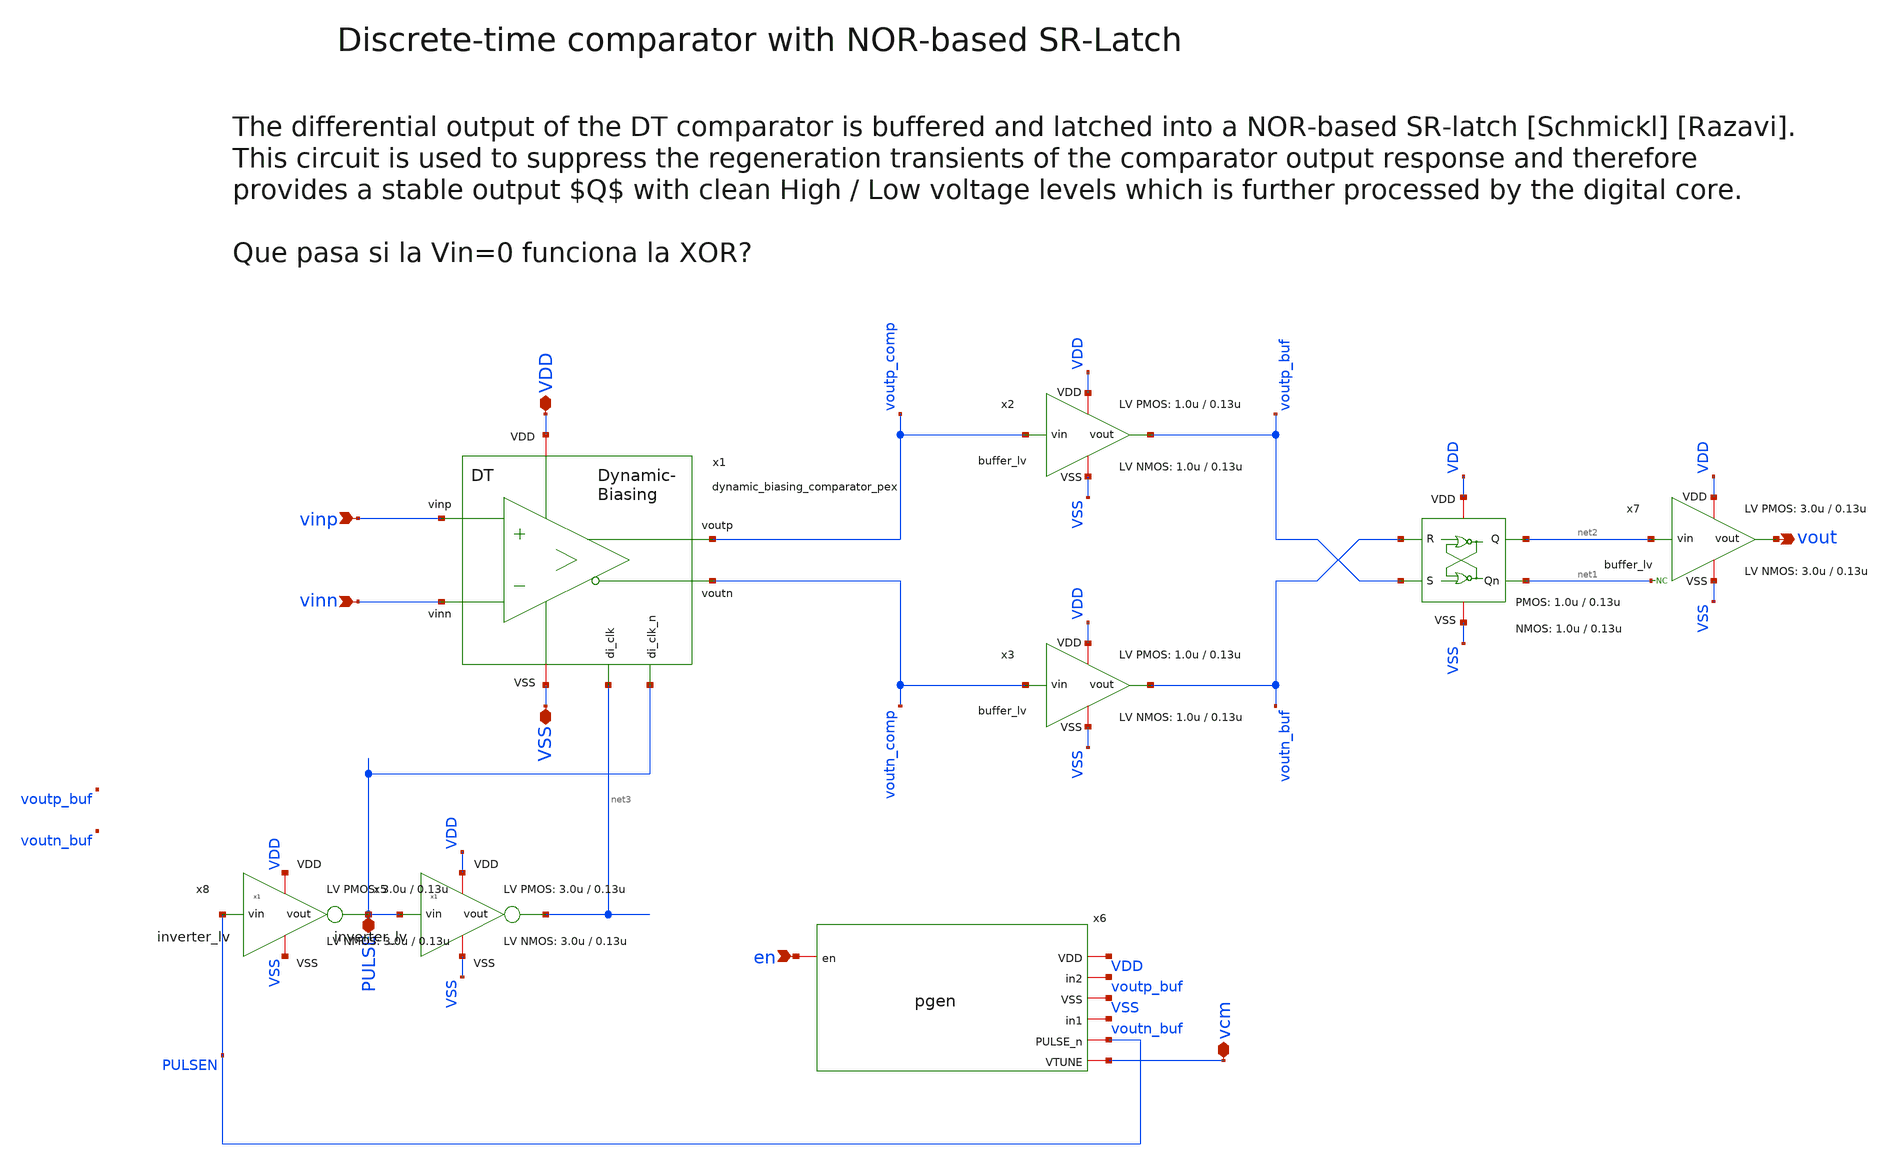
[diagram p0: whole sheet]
** sch_path: xschem/comparator/discrete_time/DT_comparator.sch
**.subckt DT_comparator VDD vout VSS vinp vinn en PULSE vcm
*.iopin VDD
*.opin vout
*.iopin VSS
*.ipin vinp
*.ipin vinn
*.ipin en
*.iopin PULSE
*.iopin vcm
x2 VDD voutp_comp voutp_buf VSS buffer_lv W_P_INV=1.0u L_P_INV=0.13u W_N_INV=1.0u L_N_INV=0.13u
x3 VDD voutn_comp voutn_buf VSS buffer_lv W_P_INV=1.0u L_P_INV=0.13u W_N_INV=1.0u L_N_INV=0.13u
x5 VDD PULSE net3 VSS inverter_lv W_P=3.0u L_P=0.13u W_N=3.0u L_N=0.13u N_C=1
* noconn #net1
x4 VDD voutp_buf net1 VSS net2 voutn_buf SR_latch W_P_SR=1.0u L_P_SR=0.13u W_N_SR=1.0u L_N_SR=0.13u
x6 VDD voutp_buf VSS voutn_buf PULSEN vcm en pgen
x1 PULSE net3 VDD voutp_comp vinp VSS voutn_comp vinn dynamic_biasing_comparator_pex
x7 VDD net2 vout VSS buffer_lv W_P_INV=3.0u L_P_INV=0.13u W_N_INV=3.0u L_N_INV=0.13u
x8 VDD PULSEN PULSE VSS inverter_lv W_P=3.0u L_P=0.13u W_N=3.0u L_N=0.13u N_C=1
**.ends
.end
